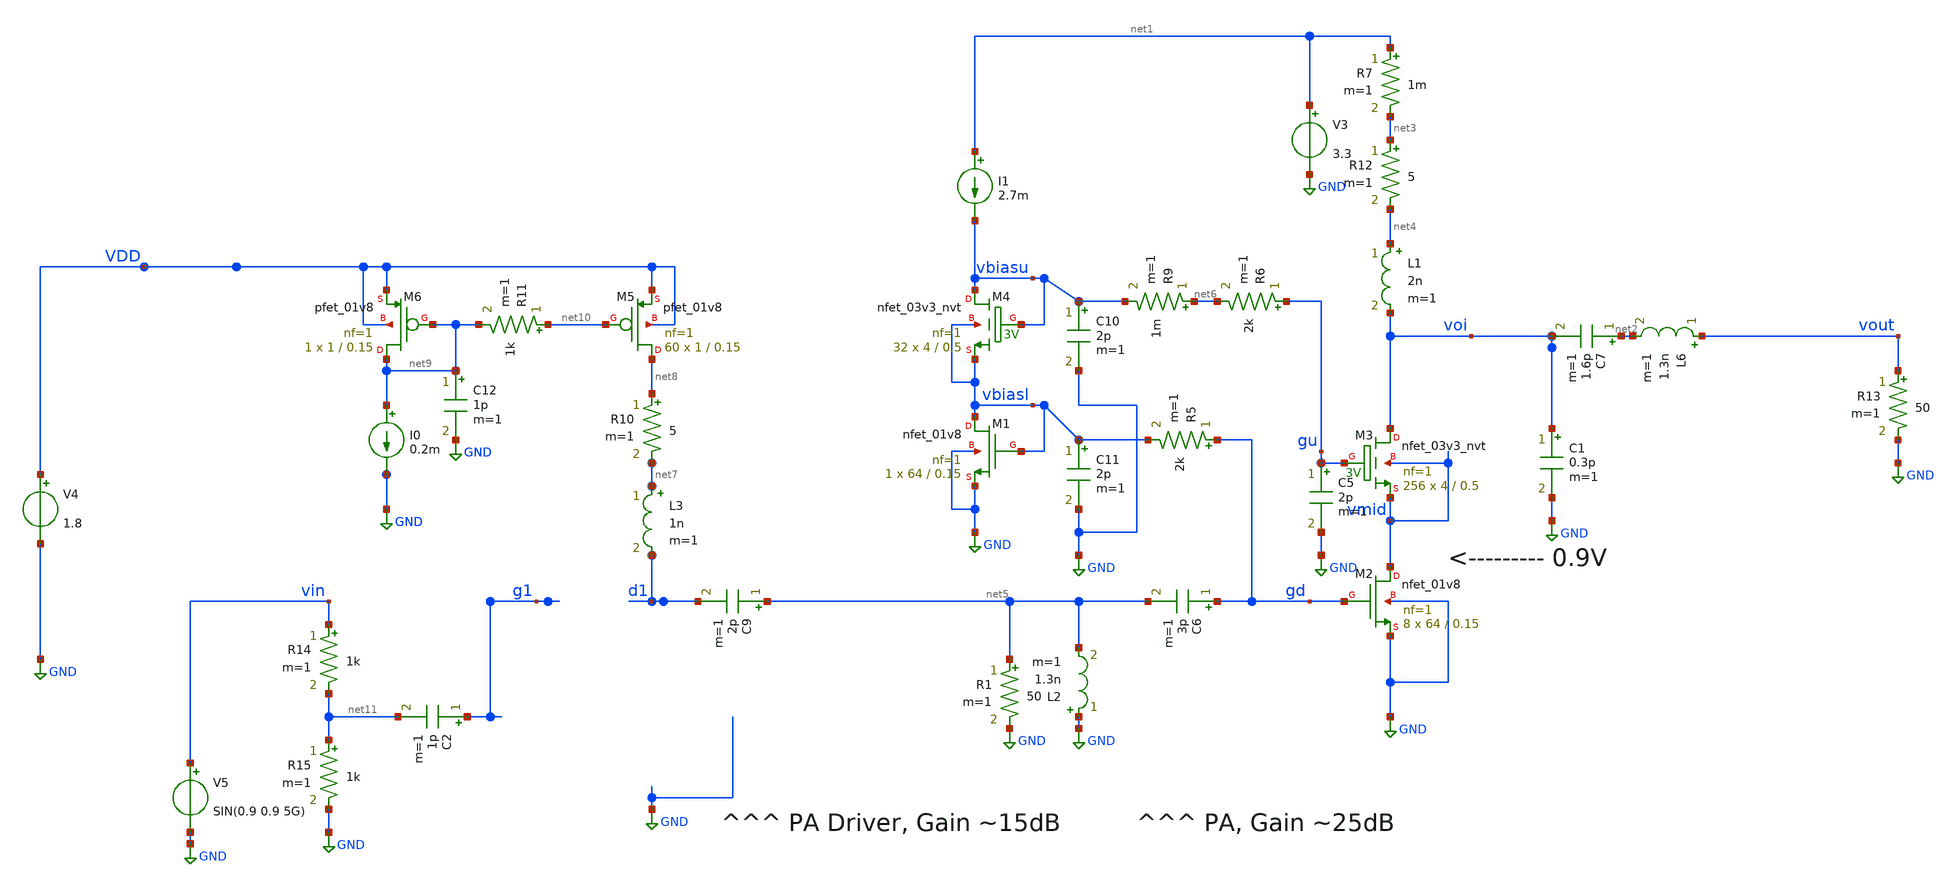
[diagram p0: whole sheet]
** sch_path: xschem/2stack_pa_complete.sch
**.subckt 2stack_pa_complete
V3 net1 GND 3.3
L1 net4 voi 2n m=1
L6 vout net2 1.3n m=1
C7 net2 voi 1.6p m=1
C1 voi GND 0.3p m=1
R5 gd vbiasl 2k m=1
XM3 voi gu vmid vmid sky130_fd_pr__nfet_03v3_nvt L=0.5 W=4 nf=1 ad='int((nf+1)/2) * W/nf * 0.29' as='int((nf+2)/2) * W/nf * 0.29'
+ pd='2*int((nf+1)/2) * (W/nf + 0.29)' ps='2*int((nf+2)/2) * (W/nf + 0.29)' nrd='0.29 / W' nrs='0.29 / W'
+ sa=0 sb=0 sd=0 mult=256 m=256
R6 gu net6 2k m=1
C5 gu GND 2p m=1
R7 net1 net3 1m m=1
XM2 vmid gd GND GND sky130_fd_pr__nfet_01v8 L=0.15 W=64 nf=1 ad='int((nf+1)/2) * W/nf * 0.29' as='int((nf+2)/2) * W/nf * 0.29'
+ pd='2*int((nf+1)/2) * (W/nf + 0.29)' ps='2*int((nf+2)/2) * (W/nf + 0.29)' nrd='0.29 / W' nrs='0.29 / W'
+ sa=0 sb=0 sd=0 mult=8 m=8
R12 net3 net4 5 m=1
C6 gd net5 3p m=1
XM1 vbiasl vbiasl GND GND sky130_fd_pr__nfet_01v8 L=0.15 W=64 nf=1 ad='int((nf+1)/2) * W/nf * 0.29' as='int((nf+2)/2) * W/nf * 0.29'
+ pd='2*int((nf+1)/2) * (W/nf + 0.29)' ps='2*int((nf+2)/2) * (W/nf + 0.29)' nrd='0.29 / W' nrs='0.29 / W'
+ sa=0 sb=0 sd=0 mult=1 m=1
XM4 vbiasu vbiasu vbiasl vbiasl sky130_fd_pr__nfet_03v3_nvt L=0.5 W=4 nf=1 ad='int((nf+1)/2) * W/nf * 0.29'
+ as='int((nf+2)/2) * W/nf * 0.29' pd='2*int((nf+1)/2) * (W/nf + 0.29)' ps='2*int((nf+2)/2) * (W/nf + 0.29)'
+ nrd='0.29 / W' nrs='0.29 / W' sa=0 sb=0 sd=0 mult=32 m=32
I1 net1 vbiasu 2.7m
C10 vbiasu GND 2p m=1
C11 vbiasl GND 2p m=1
R9 net6 vbiasu 1m m=1
R1 net5 GND 50 m=1
L2 GND net5 1.3n m=1
V4 VDD GND 1.8
V5 vin GND SIN(0.9 0.9 5G)
C2 g1 net11 1p m=1
C9 net5 d1 2p m=1
L3 net7 d1 1n m=1
R10 net8 net7 5 m=1
XM5 net8 net10 VDD VDD sky130_fd_pr__pfet_01v8 L=0.15 W=1 nf=1 ad='int((nf+1)/2) * W/nf * 0.29' as='int((nf+2)/2) * W/nf * 0.29'
+ pd='2*int((nf+1)/2) * (W/nf + 0.29)' ps='2*int((nf+2)/2) * (W/nf + 0.29)' nrd='0.29 / W' nrs='0.29 / W'
+ sa=0 sb=0 sd=0 mult=60 m=60
XM6 net9 net9 VDD VDD sky130_fd_pr__pfet_01v8 L=0.15 W=1 nf=1 ad='int((nf+1)/2) * W/nf * 0.29' as='int((nf+2)/2) * W/nf * 0.29'
+ pd='2*int((nf+1)/2) * (W/nf + 0.29)' ps='2*int((nf+2)/2) * (W/nf + 0.29)' nrd='0.29 / W' nrs='0.29 / W'
+ sa=0 sb=0 sd=0 mult=1 m=1
I0 net9 GND 0.2m
C12 net9 GND 1p m=1
R11 net10 net9 1k m=1
R14 vin net11 1k m=1
R15 net11 GND 1k m=1
R13 vout GND 50 m=1
**** begin user architecture code
.lib $::SKYWATER_MODELS/sky130.lib.spice tt
* .include $::PDKPATH/libs.ref/sky130_fd_sc_hvl/spice/sky130_fd_sc_hvl.spice


.subckt dumb_amp_core_pex NGATE NDRAIN VSUBS
.subckt sky130_fd_pr__rf_nfet_01v8_aM02W5p00L0p15 DRAIN GATE SOURCE SUBSTRATE
X0 DRAIN GATE SOURCE SUBSTRATE sky130_fd_pr__nfet_01v8 ad=1.414e+12p pd=1.066e+07u as=2.828e+12p
+ ps=2.132e+07u w=5.05e+06u l=150000u
X1 SOURCE GATE DRAIN SUBSTRATE sky130_fd_pr__nfet_01v8 ad=0p pd=0u as=0p ps=0u w=5.05e+06u l=150000u
C0 DRAIN SOURCE 3.59fF
C1 GATE SOURCE 0.46fF
C2 DRAIN GATE 0.34fF
C3 DRAIN SUBSTRATE 0.40fF
C4 SOURCE SUBSTRATE 2.44fF
C5 GATE SUBSTRATE 0.64fF
.ends
.subckt nfet_3x_2 D G S sub
Xsky130_fd_pr__rf_nfet_01v8_aM02W5p00L0p15_0 D G S sub sky130_fd_pr__rf_nfet_01v8_aM02W5p00L0p15
Xsky130_fd_pr__rf_nfet_01v8_aM02W5p00L0p15_1 D G S sub sky130_fd_pr__rf_nfet_01v8_aM02W5p00L0p15
Xsky130_fd_pr__rf_nfet_01v8_aM02W5p00L0p15_2 D G S sub sky130_fd_pr__rf_nfet_01v8_aM02W5p00L0p15
C0 G sub 1.34fF
C1 S D -0.11fF
C2 S G 2.13fF
C3 G D 1.69fF
C4 S sub -0.01fF
C5 D sub -0.05fF
C6 sub 0 -1.34fF
C7 D 0 0.62fF
C8 S 0 6.66fF
C9 G 0 1.96fF
.ends
.subckt RF_nfet_6xaM02W5p0L0p15 G S D B
Xnfet_3x_2_0 D G S B nfet_3x_2
Xnfet_3x_2_1 D G S B nfet_3x_2
C0 D B -0.02fF
C1 G S 0.20fF
C2 G B 0.06fF
C3 G D 0.14fF
C4 S B 0.02fF
C5 D S 0.01fF
C6 B 0 -3.73fF
C7 D 0 1.02fF
C8 S 0 13.03fF
C9 G 0 3.30fF
.ends
.subckt sky130_fd_pr__res_generic_po_JFYRVD a_75_284# a_n141_n357# a_n271_n487#
R0 a_n141_n357# a_75_284# sky130_fd_pr__res_generic_po w=330000u l=6.2e+06u
C0 a_n141_n357# a_n271_n487# 0.14fF
C1 a_75_284# a_n271_n487# 0.14fF
.ends
XRF_nfet_6xaM02W5p0L0p15_0 NGATE NDRAIN VSUBS VSUBS RF_nfet_6xaM02W5p0L0p15
Xsky130_fd_pr__res_generic_po_JFYRVD_0 NGATE NDRAIN VSUBS sky130_fd_pr__res_generic_po_JFYRVD
C0 VSUBS NDRAIN 1.42fF
C1 NGATE VSUBS 2.81fF
C2 NGATE NDRAIN 2.91fF
C5 NDRAIN VSUBS 14.22fF
C6 NGATE VSUBS 3.28fF
.ends

XDAPEX G1 D1 GND dumb_amp_core_pex


.options savecurrents
.tran 10ps 20ns
* .sp dec 1000 1e9 10e9 1
.control
run
display


.endc


**** end user architecture code
**.ends
.GLOBAL GND
.end
